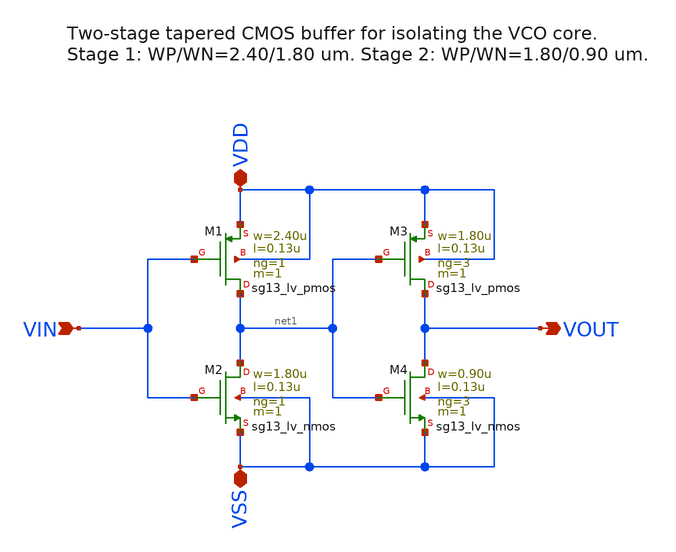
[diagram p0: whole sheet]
** sch_path: macros/pll_analog/schematic/xschem/vco_buffer.sch
**.subckt vco_buffer VIN VOUT VDD VSS
*.ipin VIN
*.opin VOUT
*.iopin VDD
*.iopin VSS
XM1 net1 VIN VDD VDD sg13_lv_pmos w=2.40u l=0.13u ng=1 m=1 mm_ok=1
XM2 net1 VIN VSS VSS sg13_lv_nmos w=1.80u l=0.13u ng=1 m=1 mm_ok=1
XM3 VOUT net1 VDD VDD sg13_lv_pmos w=1.80u l=0.13u ng=3 m=1 mm_ok=1
XM4 VOUT net1 VSS VSS sg13_lv_nmos w=0.90u l=0.13u ng=3 m=1 mm_ok=1
**.ends
.end
